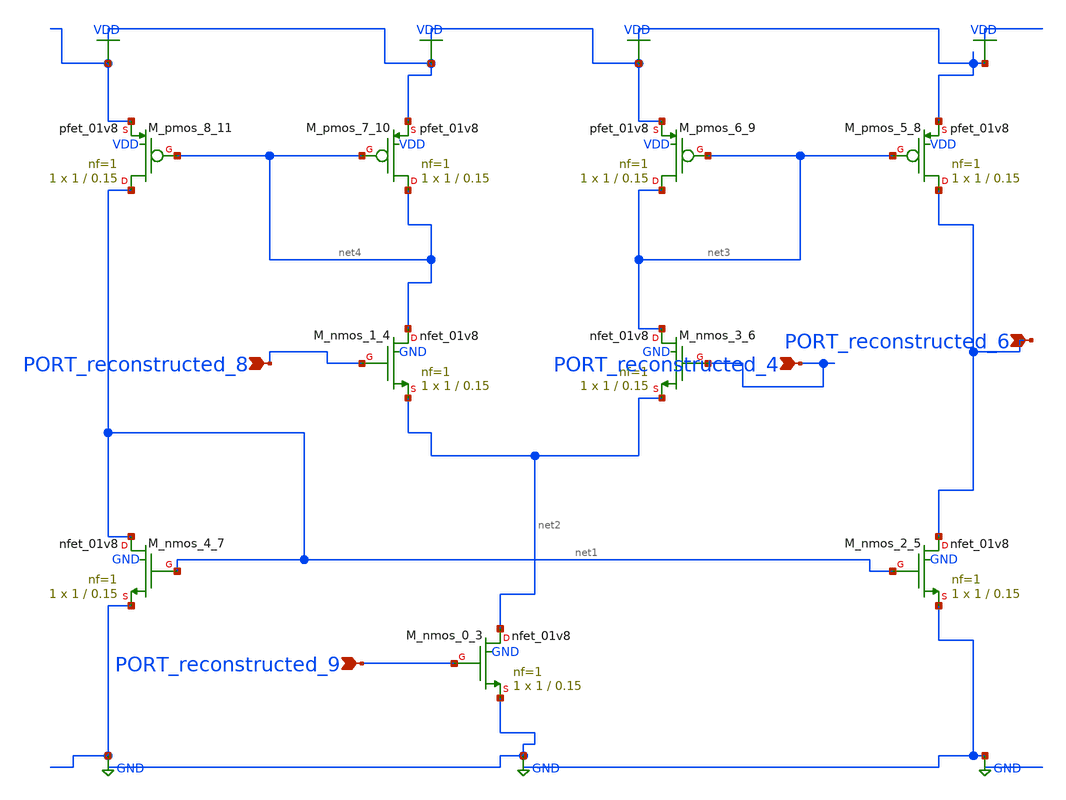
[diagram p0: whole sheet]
** sch_path: schematics/vector_p03_003_crop1.sch
**.subckt vector_p03_003_crop1 PORT_reconstructed_8 PORT_reconstructed_4 PORT_reconstructed_9
*+ PORT_reconstructed_6
*.ipin PORT_reconstructed_8
*.ipin PORT_reconstructed_4
*.ipin PORT_reconstructed_9
*.ipin PORT_reconstructed_6
XM_nmos_0_3 net2 PORT_reconstructed_9 GND GND sky130_fd_pr__nfet_01v8 L=0.15 W=1 nf=1 ad='int((1 + 1)/2) * 1 / 1 * 0.29'
+ as='int((1 + 2)/2) * 1 / 1 * 0.29' pd='2*int((1 + 1)/2) * (1 / 1 + 0.29)' ps='2*int((1 + 2)/2) * (1 / 1 + 0.29)'
+ nrd='0.29 / 1 ' nrs='0.29 / 1 ' sa=0 sb=0 sd=0 mult=1 m=1
XM_nmos_1_4 net4 PORT_reconstructed_8 net2 GND sky130_fd_pr__nfet_01v8 L=0.15 W=1 nf=1 ad='int((1 + 1)/2) * 1 / 1 * 0.29'
+ as='int((1 + 2)/2) * 1 / 1 * 0.29' pd='2*int((1 + 1)/2) * (1 / 1 + 0.29)' ps='2*int((1 + 2)/2) * (1 / 1 + 0.29)'
+ nrd='0.29 / 1 ' nrs='0.29 / 1 ' sa=0 sb=0 sd=0 mult=1 m=1
XM_nmos_2_5 PORT_reconstructed_6 net1 GND GND sky130_fd_pr__nfet_01v8 L=0.15 W=1 nf=1 ad='int((1 + 1)/2) * 1 / 1 * 0.29'
+ as='int((1 + 2)/2) * 1 / 1 * 0.29' pd='2*int((1 + 1)/2) * (1 / 1 + 0.29)' ps='2*int((1 + 2)/2) * (1 / 1 + 0.29)'
+ nrd='0.29 / 1 ' nrs='0.29 / 1 ' sa=0 sb=0 sd=0 mult=1 m=1
XM_nmos_3_6 net3 PORT_reconstructed_4 net2 GND sky130_fd_pr__nfet_01v8 L=0.15 W=1 nf=1 ad='int((1 + 1)/2) * 1 / 1 * 0.29'
+ as='int((1 + 2)/2) * 1 / 1 * 0.29' pd='2*int((1 + 1)/2) * (1 / 1 + 0.29)' ps='2*int((1 + 2)/2) * (1 / 1 + 0.29)'
+ nrd='0.29 / 1 ' nrs='0.29 / 1 ' sa=0 sb=0 sd=0 mult=1 m=1
XM_nmos_4_7 net1 net1 GND GND sky130_fd_pr__nfet_01v8 L=0.15 W=1 nf=1 ad='int((1 + 1)/2) * 1 / 1 * 0.29'
+ as='int((1 + 2)/2) * 1 / 1 * 0.29' pd='2*int((1 + 1)/2) * (1 / 1 + 0.29)' ps='2*int((1 + 2)/2) * (1 / 1 + 0.29)'
+ nrd='0.29 / 1 ' nrs='0.29 / 1 ' sa=0 sb=0 sd=0 mult=1 m=1
XM_pmos_5_8 PORT_reconstructed_6 net3 VDD VDD sky130_fd_pr__pfet_01v8 L=0.15 W=1 nf=1 ad='int((1 + 1)/2) * 1 / 1 * 0.29'
+ as='int((1 + 2)/2) * 1 / 1 * 0.29' pd='2*int((1 + 1)/2) * (1 / 1 + 0.29)' ps='2*int((1 + 2)/2) * (1 / 1 + 0.29)'
+ nrd='0.29 / 1 ' nrs='0.29 / 1 ' sa=0 sb=0 sd=0 mult=1 m=1
XM_pmos_6_9 net3 net3 VDD VDD sky130_fd_pr__pfet_01v8 L=0.15 W=1 nf=1 ad='int((1 + 1)/2) * 1 / 1 * 0.29'
+ as='int((1 + 2)/2) * 1 / 1 * 0.29' pd='2*int((1 + 1)/2) * (1 / 1 + 0.29)' ps='2*int((1 + 2)/2) * (1 / 1 + 0.29)'
+ nrd='0.29 / 1 ' nrs='0.29 / 1 ' sa=0 sb=0 sd=0 mult=1 m=1
XM_pmos_7_10 net4 net4 VDD VDD sky130_fd_pr__pfet_01v8 L=0.15 W=1 nf=1 ad='int((1 + 1)/2) * 1 / 1 * 0.29'
+ as='int((1 + 2)/2) * 1 / 1 * 0.29' pd='2*int((1 + 1)/2) * (1 / 1 + 0.29)' ps='2*int((1 + 2)/2) * (1 / 1 + 0.29)'
+ nrd='0.29 / 1 ' nrs='0.29 / 1 ' sa=0 sb=0 sd=0 mult=1 m=1
XM_pmos_8_11 net1 net4 VDD VDD sky130_fd_pr__pfet_01v8 L=0.15 W=1 nf=1 ad='int((1 + 1)/2) * 1 / 1 * 0.29'
+ as='int((1 + 2)/2) * 1 / 1 * 0.29' pd='2*int((1 + 1)/2) * (1 / 1 + 0.29)' ps='2*int((1 + 2)/2) * (1 / 1 + 0.29)'
+ nrd='0.29 / 1 ' nrs='0.29 / 1 ' sa=0 sb=0 sd=0 mult=1 m=1
**.ends
.GLOBAL GND
.GLOBAL VDD
.end
